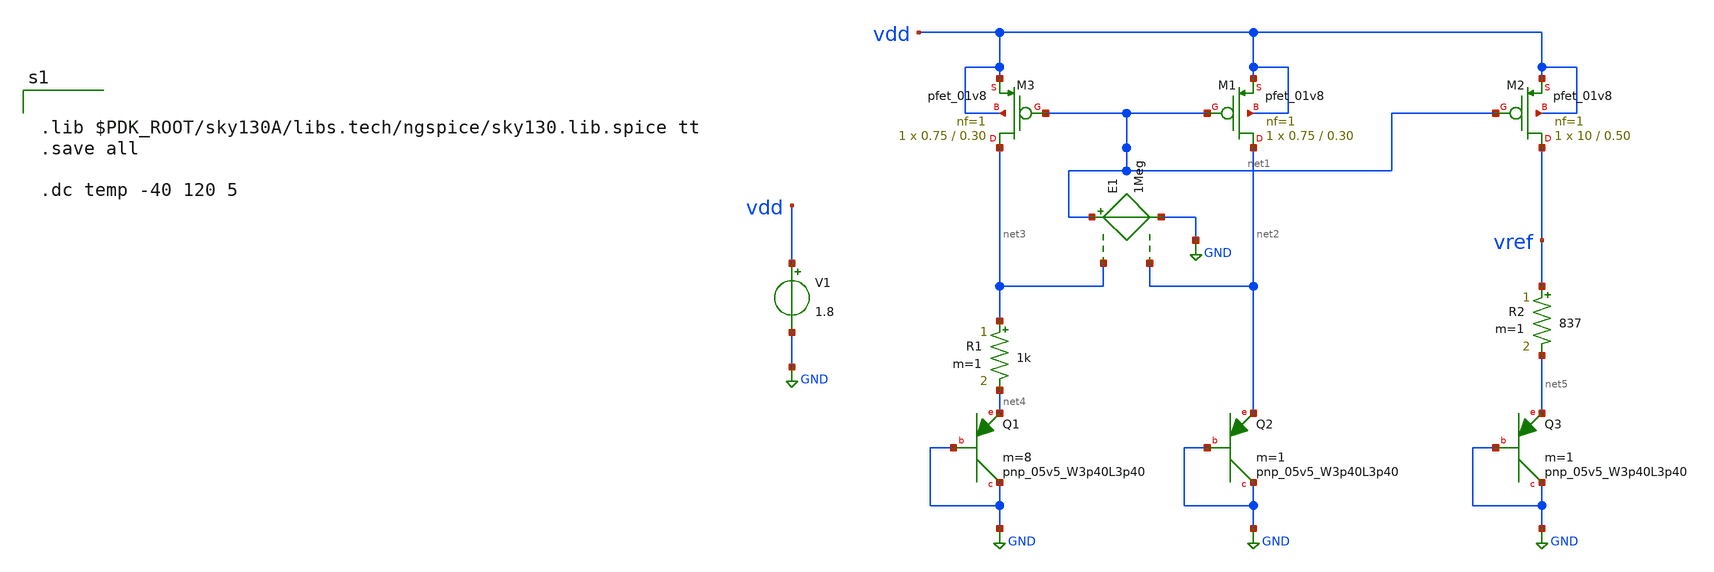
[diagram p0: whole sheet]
** sch_path: Bandgap/schem.sch
**.subckt schem
R1 net3 net4 1k m=1
E1 net1 GND net3 net2 1Meg
V1 vdd GND 1.8
R2 vref net5 837 m=1
XM1 net2 net1 vdd vdd sky130_fd_pr__pfet_01v8 L=0.30 W=0.75 nf=1 ad='int((1 + 1)/2) * 0.75 / 1 * 0.29'
+ as='int((1 + 2)/2) * 0.75 / 1 * 0.29' pd='2*int((1 + 1)/2) * (0.75 / 1 + 0.29)' ps='2*int((1 + 2)/2) * (0.75 / 1 + 0.29)'
+ nrd='0.29 / 0.75 ' nrs='0.29 / 0.75 ' sa=0 sb=0 sd=0 mult=1 m=1
XM2 vref net1 vdd vdd sky130_fd_pr__pfet_01v8 L=0.50 W=10 nf=1 ad='int((1 + 1)/2) * 10 / 1 * 0.29' as='int((1 + 2)/2) * 10 / 1 * 0.29'
+ pd='2*int((1 + 1)/2) * (10 / 1 + 0.29)' ps='2*int((1 + 2)/2) * (10 / 1 + 0.29)' nrd='0.29 / 10 ' nrs='0.29 / 10 '
+ sa=0 sb=0 sd=0 mult=1 m=1
XM3 net3 net1 vdd vdd sky130_fd_pr__pfet_01v8 L=0.30 W=0.75 nf=1 ad='int((1 + 1)/2) * 0.75 / 1 * 0.29'
+ as='int((1 + 2)/2) * 0.75 / 1 * 0.29' pd='2*int((1 + 1)/2) * (0.75 / 1 + 0.29)' ps='2*int((1 + 2)/2) * (0.75 / 1 + 0.29)'
+ nrd='0.29 / 0.75 ' nrs='0.29 / 0.75 ' sa=0 sb=0 sd=0 mult=1 m=1
XQ1 GND GND net4 sky130_fd_pr__pnp_05v5_W3p40L3p40 m=8
XQ2 GND GND net2 sky130_fd_pr__pnp_05v5_W3p40L3p40 m=1
XQ3 GND GND net5 sky130_fd_pr__pnp_05v5_W3p40L3p40 m=1
**** begin user architecture code


.lib $PDK_ROOT/sky130A/libs.tech/ngspice/sky130.lib.spice tt
.save all

.dc temp -40 120 5


**** end user architecture code
**.ends
.GLOBAL GND
.end
